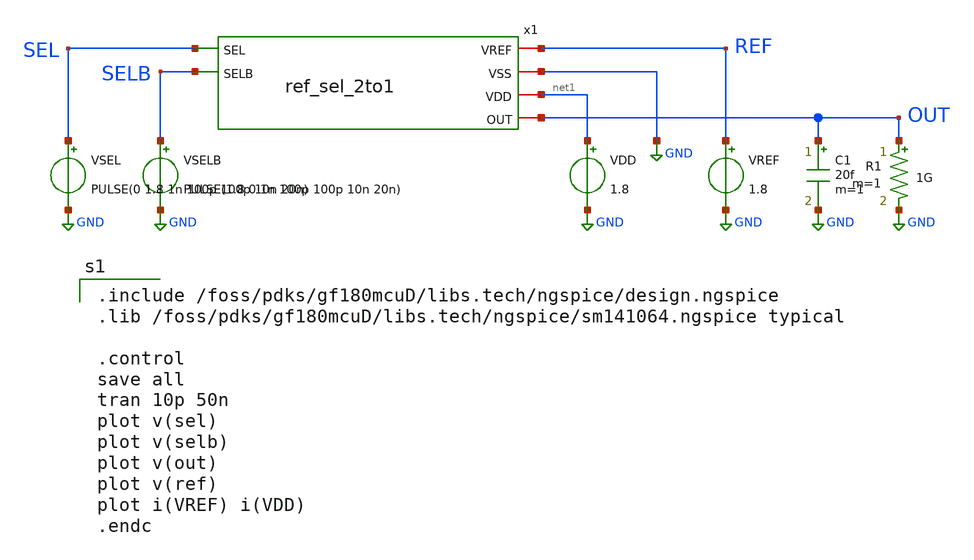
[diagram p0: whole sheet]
** sch_path: designs/libs/tb_matchmaker/tb_ref_sel_2to1/tb_ref_sel_2to1.sch
**.subckt tb_ref_sel_2to1
x1 SEL REF GND SELB net1 OUT ref_sel_2to1
VDD net1 GND 1.8
VREF REF GND 1.8
C1 OUT GND 20f m=1
R1 OUT GND 1G m=1
VSELB SELB GND PULSE(1.8 0 1n 100p 100p 10n 20n)
VSEL SEL GND PULSE(0 1.8 1n 100p 100p 10n 20n)
**** begin user architecture code

.include /foss/pdks/gf180mcuD/libs.tech/ngspice/design.ngspice
.lib /foss/pdks/gf180mcuD/libs.tech/ngspice/sm141064.ngspice typical

.control
save all
tran 10p 50n
plot v(sel)
plot v(selb)
plot v(out)
plot v(ref)
plot i(VREF) i(VDD)
.endc

**** end user architecture code
**.ends
.GLOBAL GND
.end
